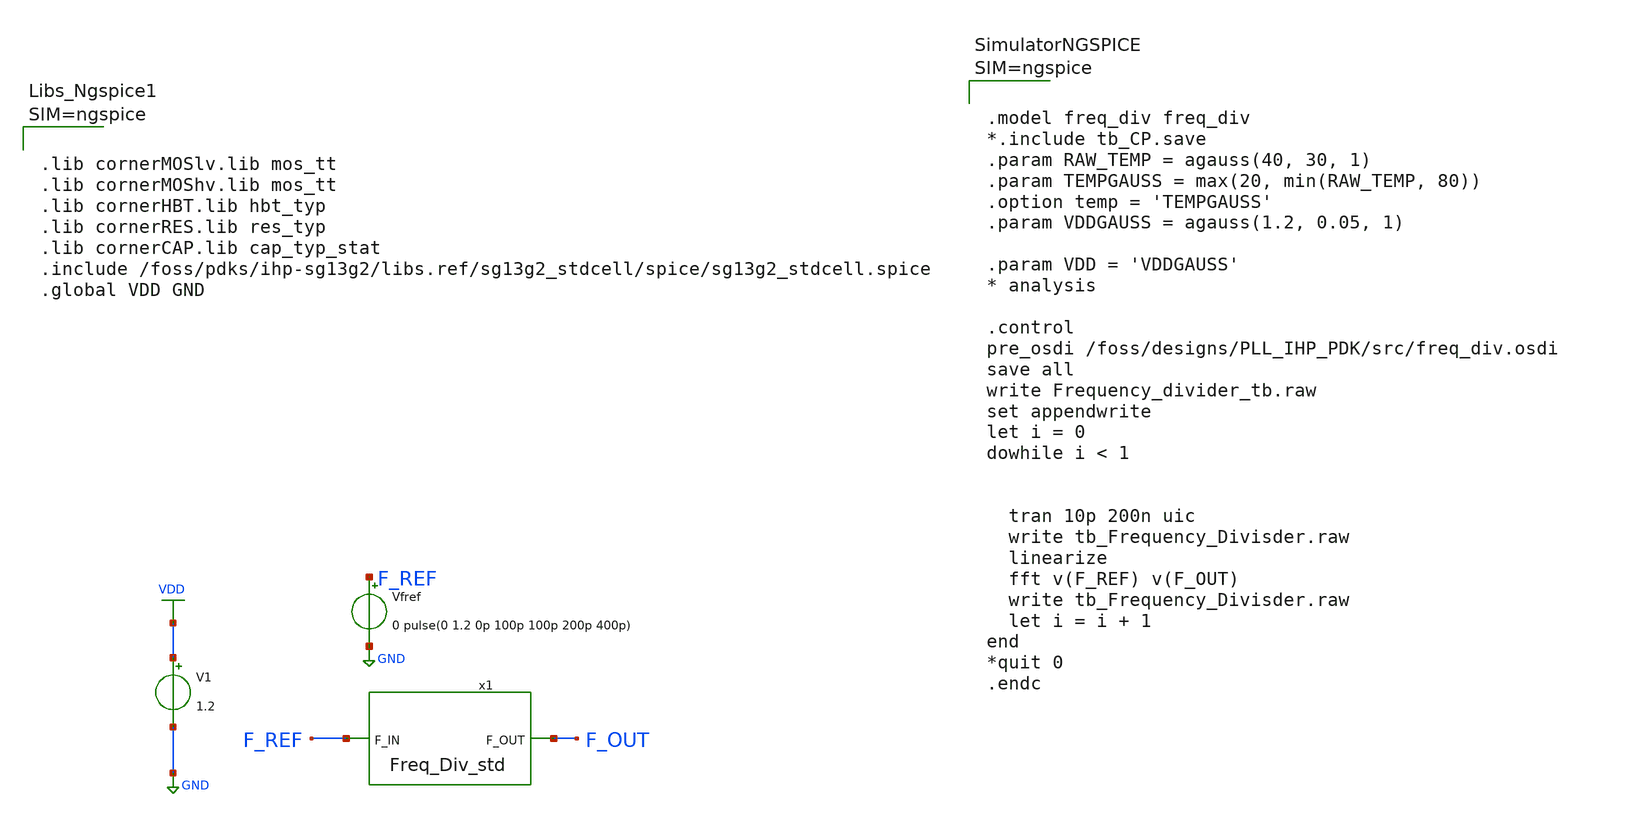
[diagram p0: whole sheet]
** sch_path: xschem/Test/FD/Frequency_Divider_tb.sch
**.subckt Frequency_Divider_tb
V1 VDD GND 1.2
Vfref F_REF GND 0 pulse(0 1.2 0p 100p 100p 200p 400p)
x1 F_REF F_OUT Freq_Div_std
**** begin user architecture code



.model freq_div freq_div
*.include tb_CP.save
.param RAW_TEMP = agauss(40, 30, 1)
.param TEMPGAUSS = max(20, min(RAW_TEMP, 80))
.option temp = 'TEMPGAUSS'
.param VDDGAUSS = agauss(1.2, 0.05, 1)

.param VDD = 'VDDGAUSS'
* analysis

.control
pre_osdi /foss/designs/PLL_IHP_PDK/src/freq_div.osdi
save all
write Frequency_divider_tb.raw
set appendwrite
let i = 0
dowhile i < 1


  tran 10p 200n uic
  write tb_Frequency_Divisder.raw
  linearize
  fft v(F_REF) v(F_OUT)
  write tb_Frequency_Divisder.raw
  let i = i + 1
end
*quit 0
.endc






.lib cornerMOSlv.lib mos_tt
.lib cornerMOShv.lib mos_tt
.lib cornerHBT.lib hbt_typ
.lib cornerRES.lib res_typ
.lib cornerCAP.lib cap_typ_stat
.include /foss/pdks/ihp-sg13g2/libs.ref/sg13g2_stdcell/spice/sg13g2_stdcell.spice
.global VDD GND



**** end user architecture code
**.ends

* expanding   symbol:  Freq_Div_std.sym # of pins=2
** sym_path: schematic/Test/FD/Freq_Div_std.sym
** sch_path: schematic/Test/FD/Freq_Div_std.sch
.subckt Freq_Div_std F_IN F_OUT
*.opin F_OUT
*.ipin F_IN
x6 net3 net1 F_IN net1 VDD VDD GND sg13g2_dfrbp_1
x5 net4 net2 net3 net2 VDD VDD GND sg13g2_dfrbp_2
x7 net6 net5 net4 net5 VDD VDD GND sg13g2_dfrbp_2
x8 F_OUT net7 net6 net7 VDD VDD GND sg13g2_dfrbp_2
.ends


* expanding   symbol:  sg13g2_stdcells/sg13g2_dfrbp_1.sym # of pins=5
** sym_path: sg13g2_stdcells/sg13g2_dfrbp_1.sym
** sch_path: sg13g2_stdcells/sg13g2_dfrbp_1.sch
.subckt sg13g2_dfrbp_1 Q Q_N CLK D RESET_B VDD VSS
*.ipin D
*.ipin RESET_B
*.ipin CLK
*.opin Q
*.opin Q_N
*.iopin VDD
*.iopin VSS
XM1 Db D net10 VSS sg13_lv_nmos w=420.00n l=130.00n ng=1 m=1 mm_ok=1
XM2 net10 RESET_B VSS VSS sg13_lv_nmos w=420.00n l=130.00n ng=1 m=1 mm_ok=1
XM3 net1 clkneg net9 VSS sg13_lv_nmos w=420.00n l=130.00n ng=1 m=1 mm_ok=1
XM4 net9 net1 VSS VSS sg13_lv_nmos w=420.00n l=130.00n ng=1 m=1 mm_ok=1
XM5 net1 net1 net5 VSS sg13_lv_nmos w=420.00n l=130.00n ng=1 m=1 mm_ok=1
XM6 net5 RESET_B VSS VSS sg13_lv_nmos w=420.00n l=130.00n ng=1 m=1 mm_ok=1
XM7 Q_N net1 VSS VSS sg13_lv_nmos w=740.00n l=130.00n ng=1 m=1 mm_ok=1
XM8 net2 net1 VSS VSS sg13_lv_nmos w=740.00n l=130.00n ng=1 m=1 mm_ok=1
XM9 Q net2 VSS VSS sg13_lv_nmos w=740.00n l=130.00n ng=1 m=1 mm_ok=1
XM10 clkneg CLK VSS VSS sg13_lv_nmos w=740.00n l=130.00n ng=1 m=1 mm_ok=1
XM11 clkpos clkneg VSS VSS sg13_lv_nmos w=740.00n l=130.00n ng=1 m=1 mm_ok=1
XM12 Db clkneg net3 VSS sg13_lv_nmos w=420.00n l=130.00n ng=1 m=1 mm_ok=1
XM13 net3 clkpos net8 VSS sg13_lv_nmos w=420.00n l=130.00n ng=1 m=1 mm_ok=1
XM14 net8 net3 net4 VSS sg13_lv_nmos w=420.00n l=130.00n ng=1 m=1 mm_ok=1
XM15 net4 RESET_B VSS VSS sg13_lv_nmos w=420.00n l=130.00n ng=1 m=1 mm_ok=1
XM16 net3 net3 VSS VSS sg13_lv_nmos w=740.00n l=130.00n ng=1 m=1 mm_ok=1
XM17 net3 clkpos net1 VSS sg13_lv_nmos w=740.00n l=130.00n ng=1 m=1 mm_ok=1
XM18 Db RESET_B VDD VDD sg13_lv_pmos w=420.00n l=130.00n ng=1 m=1 mm_ok=1
XM19 Db D VDD VDD sg13_lv_pmos w=420.00n l=130.00n ng=1 m=1 mm_ok=1
XM20 net7 net1 VDD VDD sg13_lv_pmos w=420.00n l=130.00n ng=1 m=1 mm_ok=1
XM21 net1 clkpos net7 VDD sg13_lv_pmos w=420.00n l=130.00n ng=1 m=1 mm_ok=1
XM22 net1 net1 VDD VDD sg13_lv_pmos w=420.00n l=130.00n ng=1 m=1 mm_ok=1
XM23 net1 RESET_B VDD VDD sg13_lv_pmos w=420.00n l=130.00n ng=1 m=1 mm_ok=1
XM24 Q_N net1 VDD VDD sg13_lv_pmos w=1.12u l=130.00n ng=1 m=1 mm_ok=1
XM25 net2 net1 VDD VDD sg13_lv_pmos w=1.12u l=130.00n ng=1 m=1 mm_ok=1
XM26 Q net2 VDD VDD sg13_lv_pmos w=1.12u l=130.00n ng=1 m=1 mm_ok=1
XM27 clkneg CLK VDD VDD sg13_lv_pmos w=1.12u l=130.00n ng=1 m=1 mm_ok=1
XM28 clkpos clkneg VDD VDD sg13_lv_pmos w=1.12u l=130.00n ng=1 m=1 mm_ok=1
XM29 Db clkpos net3 VDD sg13_lv_pmos w=420.00n l=130.00n ng=1 m=1 mm_ok=1
XM30 net6 net3 VDD VDD sg13_lv_pmos w=420.00n l=130.00n ng=1 m=1 mm_ok=1
XM31 net3 clkneg net6 VDD sg13_lv_pmos w=420.00n l=130.00n ng=1 m=1 mm_ok=1
XM32 net3 RESET_B VDD VDD sg13_lv_pmos w=420.00n l=130.00n ng=1 m=1 mm_ok=1
XM33 net3 net3 VDD VDD sg13_lv_pmos w=1.000u l=130.00n ng=1 m=1 mm_ok=1
XM34 net3 clkneg net1 VDD sg13_lv_pmos w=1.000u l=130.00n ng=1 m=1 mm_ok=1
.ends

.GLOBAL GND
.GLOBAL VDD
.end
